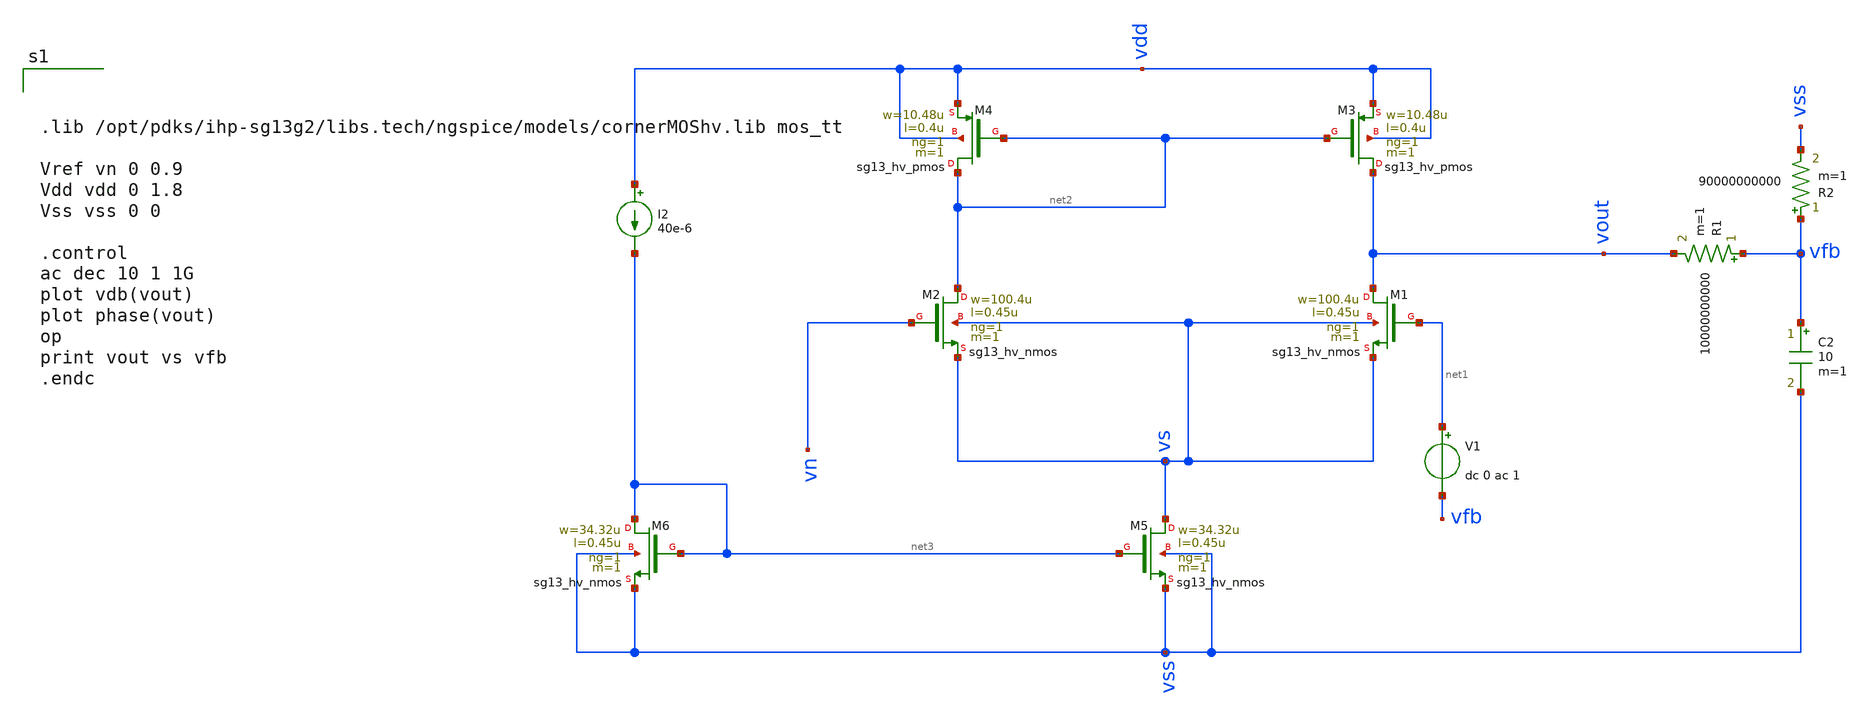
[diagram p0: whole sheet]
** sch_path: test/Tesis_notebooks/xschem/ota_1stage_tb.sch
**.subckt ota_1stage_tb
XM1 vout net1 vs vs sg13_hv_nmos w=100.4u l=0.45u ng=1 m=1 mm_ok=1
XM2 net2 vn vs vs sg13_hv_nmos w=100.4u l=0.45u ng=1 m=1 mm_ok=1
XM3 vout net2 vdd vdd sg13_hv_pmos w=10.48u l=0.4u ng=1 m=1 mm_ok=1
XM4 net2 net2 vdd vdd sg13_hv_pmos w=10.48u l=0.4u ng=1 m=1 mm_ok=1
R1 vfb vout 10000000000 m=1
C2 vfb vss 10 m=1
R2 vfb vss 90000000000 m=1
XM5 vs net3 vss vss sg13_hv_nmos w=34.32u l=0.45u ng=1 m=1 mm_ok=1
XM6 net3 net3 vss vss sg13_hv_nmos w=34.32u l=0.45u ng=1 m=1 mm_ok=1
I2 vdd net3 40e-6
V1 net1 vfb dc 0 ac 1
**** begin user architecture code



.lib /opt/pdks/ihp-sg13g2/libs.tech/ngspice/models/cornerMOShv.lib mos_tt

Vref vn 0 0.9
Vdd vdd 0 1.8
Vss vss 0 0

.control
ac dec 10 1 1G
plot vdb(vout)
plot phase(vout)
op
print vout vs vfb
.endc



**** end user architecture code
**.ends
.end
